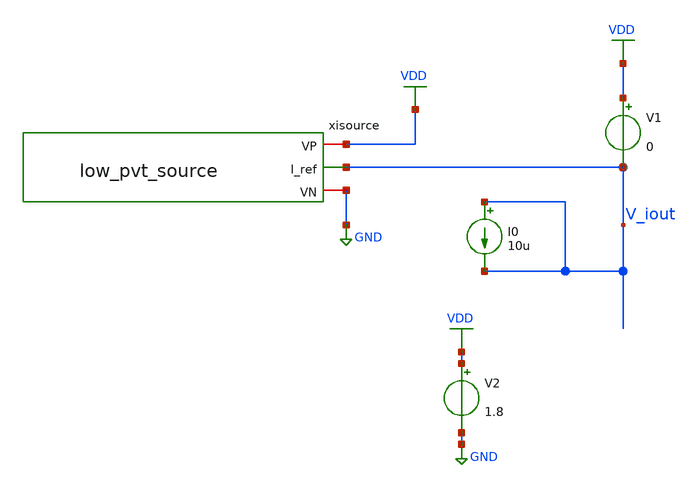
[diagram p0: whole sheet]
** sch_path: xschem/test/test_low_pvt_source.sch
**.subckt test_low_pvt_source
V2 VDD GND 1.8
V1 VDD V_iout 0
xisource VDD V_iout GND low_pvt_source
I0 V_iout V_iout 10u
**** begin user architecture code


*.options savecurrents
.option warn=1
.control
set wr_vecnames
set wr_singlescale
set hcopydevtype=svg
set ITL1=10000

let min_temp=0
let var_temp = min_temp
let max_temp=100
let temp_step=100

option temp=20
op
write test_low_pvt_source.raw
print var_temp i(v1)
*  i(v.xisource.v1)
run
reset



dowhile var_temp <= max_temp
	option temp=$&var_temp
	op
	* wrdata 'result_{$&var_temp}deg.csv' v(V_vout)
	let var_temp = var_temp + temp_step
	run
	echo 'Result will follow ...'
	print var_temp  i(v1)
	* i(v.xisource.v1)
	if i(v.xisource.v1) > 1e-6
		echo 'Large current'
		write 'result_op_{$&var_temp}deg.raw'
	end
	*tran 100n 100u
	*MEAS tran isource AVG i(v.xisource.v1) from=50u to=100u
	reset
end

* reset
* option temp=0
* op
* run
* print v(v_vout) i(v1)
* let var_vout_0deg=v(v_vout)
* reset
* option temp=100
* op
* run
* print v(v_vout) i(v1)
* let var_vout_100deg=v(v_vout)

* print var_vout_100deg-var_vout_0deg

* tran 100n 100u
* plot i(v.xisource.v1)
* MEAS tran isource AVG i(v.xisource.v1) from=50u to=100u
* noise i(v1) I0 dec 1000 10 100G
* print all
* wrdata result_noise.csv inoise_total onoise_total
* setplot noise1
* plot onoise_spectrum
* noise i(v1) I0 dec 1000 2MEG 2G
* print all
* wrdata result_noise.csv inoise_total onoise_total
* setplot noise3
* plot onoise_spectrum


.endc




* .include ../../tia.spice
* .include ../../filter_diff.spice
* .include ../../cmm_sense3.spice

.include low_pvt_source.spice



* .lib $::SKYWATER_MODELS/sky130.lib.spice hl
.lib $::SKYWATER_MODELS/sky130.lib.spice.tt.red tt
* .lib /home/simon/share/pdk/sky130A/libs.tech/ngspice/sky130.lib.spice.tt.red tt

**** end user architecture code
**.ends

* expanding   symbol:  /home/simon/code/asic/analog/bias/low_pvt_source.sym # of pins=3
** sym_path: xschem/bias/low_pvt_source.sym
** sch_path: xschem/bias/low_pvt_source.sch
.subckt low_pvt_source VP I_ref VN
*.iopin VP
*.opin I_ref
*.iopin VN
XM1 VM1D VM8D VP VP sky130_fd_pr__pfet_01v8 L=1 W=4 nf=1 ad='int((nf+1)/2) * W/nf * 0.29' as='int((nf+2)/2) * W/nf * 0.29'
+ pd='2*int((nf+1)/2) * (W/nf + 0.29)' ps='2*int((nf+2)/2) * (W/nf + 0.29)' nrd='0.29 / W' nrs='0.29 / W'
+ sa=0 sb=0 sd=0 mult=10 m=10
XM2 VM2D VM2D VN VN sky130_fd_pr__nfet_01v8 L=6 W=4 nf=1 ad='int((nf+1)/2) * W/nf * 0.29' as='int((nf+2)/2) * W/nf * 0.29'
+ pd='2*int((nf+1)/2) * (W/nf + 0.29)' ps='2*int((nf+2)/2) * (W/nf + 0.29)' nrd='0.29 / W' nrs='0.29 / W'
+ sa=0 sb=0 sd=0 mult=30 m=30
XM5 VM9D VM8D VM1D VP sky130_fd_pr__pfet_01v8 L=0.2 W=4 nf=1 ad='int((nf+1)/2) * W/nf * 0.29' as='int((nf+2)/2) * W/nf * 0.29'
+ pd='2*int((nf+1)/2) * (W/nf + 0.29)' ps='2*int((nf+2)/2) * (W/nf + 0.29)' nrd='0.29 / W' nrs='0.29 / W'
+ sa=0 sb=0 sd=0 mult=2 m=2
XM11 VM11D VM2D VM12D VN sky130_fd_pr__nfet_01v8 L=6 W=4 nf=1 ad='int((nf+1)/2) * W/nf * 0.29' as='int((nf+2)/2) * W/nf * 0.29'
+ pd='2*int((nf+1)/2) * (W/nf + 0.29)' ps='2*int((nf+2)/2) * (W/nf + 0.29)' nrd='0.29 / W' nrs='0.29 / W'
+ sa=0 sb=0 sd=0 mult=65 m=65
XM12 VM12D VM12G VN VN sky130_fd_pr__nfet_01v8 L=6 W=4 nf=1 ad='int((nf+1)/2) * W/nf * 0.29' as='int((nf+2)/2) * W/nf * 0.29'
+ pd='2*int((nf+1)/2) * (W/nf + 0.29)' ps='2*int((nf+2)/2) * (W/nf + 0.29)' nrd='0.29 / W' nrs='0.29 / W'
+ sa=0 sb=0 sd=0 mult=2 m=2
XM14 VM14D VM12G VN VN sky130_fd_pr__nfet_01v8 L=6 W=4 nf=1 ad='int((nf+1)/2) * W/nf * 0.29' as='int((nf+2)/2) * W/nf * 0.29'
+ pd='2*int((nf+1)/2) * (W/nf + 0.29)' ps='2*int((nf+2)/2) * (W/nf + 0.29)' nrd='0.29 / W' nrs='0.29 / W'
+ sa=0 sb=0 sd=0 mult=2 m=2
XM16 VM16D VM8D VP VP sky130_fd_pr__pfet_01v8 L=1 W=4 nf=1 ad='int((nf+1)/2) * W/nf * 0.29' as='int((nf+2)/2) * W/nf * 0.29'
+ pd='2*int((nf+1)/2) * (W/nf + 0.29)' ps='2*int((nf+2)/2) * (W/nf + 0.29)' nrd='0.29 / W' nrs='0.29 / W'
+ sa=0 sb=0 sd=0 mult=10 m=10
XM17 VM8D VM8D VM16D VP sky130_fd_pr__pfet_01v8 L=0.2 W=4 nf=1 ad='int((nf+1)/2) * W/nf * 0.29' as='int((nf+2)/2) * W/nf * 0.29'
+ pd='2*int((nf+1)/2) * (W/nf + 0.29)' ps='2*int((nf+2)/2) * (W/nf + 0.29)' nrd='0.29 / W' nrs='0.29 / W'
+ sa=0 sb=0 sd=0 mult=2 m=2
XM18 VM18D VM8D VP VP sky130_fd_pr__pfet_01v8 L=1 W=4 nf=1 ad='int((nf+1)/2) * W/nf * 0.29' as='int((nf+2)/2) * W/nf * 0.29'
+ pd='2*int((nf+1)/2) * (W/nf + 0.29)' ps='2*int((nf+2)/2) * (W/nf + 0.29)' nrd='0.29 / W' nrs='0.29 / W'
+ sa=0 sb=0 sd=0 mult=10*3*2 m=10*3*2
XM19 VM14D VM8D VM18D VP sky130_fd_pr__pfet_01v8 L=0.2 W=4 nf=1 ad='int((nf+1)/2) * W/nf * 0.29' as='int((nf+2)/2) * W/nf * 0.29'
+ pd='2*int((nf+1)/2) * (W/nf + 0.29)' ps='2*int((nf+2)/2) * (W/nf + 0.29)' nrd='0.29 / W' nrs='0.29 / W'
+ sa=0 sb=0 sd=0 mult=2*3*2 m=2*3*2
XM20 VM20D VM8D VP VP sky130_fd_pr__pfet_01v8 L=1 W=4 nf=1 ad='int((nf+1)/2) * W/nf * 0.29' as='int((nf+2)/2) * W/nf * 0.29'
+ pd='2*int((nf+1)/2) * (W/nf + 0.29)' ps='2*int((nf+2)/2) * (W/nf + 0.29)' nrd='0.29 / W' nrs='0.29 / W'
+ sa=0 sb=0 sd=0 mult=10*1*1 m=10*1*1
XM21 VM22D VM8D VM20D VP sky130_fd_pr__pfet_01v8 L=0.2 W=4 nf=1 ad='int((nf+1)/2) * W/nf * 0.29' as='int((nf+2)/2) * W/nf * 0.29'
+ pd='2*int((nf+1)/2) * (W/nf + 0.29)' ps='2*int((nf+2)/2) * (W/nf + 0.29)' nrd='0.29 / W' nrs='0.29 / W'
+ sa=0 sb=0 sd=0 mult=2*1*1 m=2*1*1
XM22 VM22D VM4S VM3D VN sky130_fd_pr__nfet_01v8 L=6 W=4 nf=1 ad='int((nf+1)/2) * W/nf * 0.29' as='int((nf+2)/2) * W/nf * 0.29'
+ pd='2*int((nf+1)/2) * (W/nf + 0.29)' ps='2*int((nf+2)/2) * (W/nf + 0.29)' nrd='0.29 / W' nrs='0.29 / W'
+ sa=0 sb=0 sd=0 mult=20 m=20
XM3 VM3D VM3G VN VN sky130_fd_pr__nfet_01v8 L=6 W=4 nf=1 ad='int((nf+1)/2) * W/nf * 0.29' as='int((nf+2)/2) * W/nf * 0.29'
+ pd='2*int((nf+1)/2) * (W/nf + 0.29)' ps='2*int((nf+2)/2) * (W/nf + 0.29)' nrd='0.29 / W' nrs='0.29 / W'
+ sa=0 sb=0 sd=0 mult=4 m=4
XM13 VP VM14D VM12G VM12G sky130_fd_pr__nfet_01v8_lvt L=0.15 W=4 nf=1 ad='int((nf+1)/2) * W/nf * 0.29'
+ as='int((nf+2)/2) * W/nf * 0.29' pd='2*int((nf+1)/2) * (W/nf + 0.29)' ps='2*int((nf+2)/2) * (W/nf + 0.29)'
+ nrd='0.29 / W' nrs='0.29 / W' sa=0 sb=0 sd=0 mult=20 m=20
XM4 I_ref VM22D VM4S VN sky130_fd_pr__nfet_01v8_lvt L=0.15 W=4 nf=1 ad='int((nf+1)/2) * W/nf * 0.29'
+ as='int((nf+2)/2) * W/nf * 0.29' pd='2*int((nf+1)/2) * (W/nf + 0.29)' ps='2*int((nf+2)/2) * (W/nf + 0.29)'
+ nrd='0.29 / W' nrs='0.29 / W' sa=0 sb=0 sd=0 mult=20 m=20
XM48 VM50D VM11D VP VP sky130_fd_pr__pfet_01v8 L=2 W=0.5 nf=1 ad='int((nf+1)/2) * W/nf * 0.29' as='int((nf+2)/2) * W/nf * 0.29'
+ pd='2*int((nf+1)/2) * (W/nf + 0.29)' ps='2*int((nf+2)/2) * (W/nf + 0.29)' nrd='0.29 / W' nrs='0.29 / W'
+ sa=0 sb=0 sd=0 mult=1 m=1
XM50 VM50D VM11D VN VN sky130_fd_pr__nfet_01v8_lvt L=0.2 W=4 nf=1 ad='int((nf+1)/2) * W/nf * 0.29' as='int((nf+2)/2) * W/nf * 0.29'
+ pd='2*int((nf+1)/2) * (W/nf + 0.29)' ps='2*int((nf+2)/2) * (W/nf + 0.29)' nrd='0.29 / W' nrs='0.29 / W'
+ sa=0 sb=0 sd=0 mult=10 m=10
XC3 VP VM8D sky130_fd_pr__cap_mim_m3_1 W=20 L=20 MF=1 m=1
XM8 VM8D VM9D VM11D VM11D sky130_fd_pr__nfet_01v8_lvt L=1 W=4 nf=1 ad='int((nf+1)/2) * W/nf * 0.29' as='int((nf+2)/2) * W/nf * 0.29'
+ pd='2*int((nf+1)/2) * (W/nf + 0.29)' ps='2*int((nf+2)/2) * (W/nf + 0.29)' nrd='0.29 / W' nrs='0.29 / W'
+ sa=0 sb=0 sd=0 mult=20 m=20
XM9 VM9D VM9D VM2D VM2D sky130_fd_pr__nfet_01v8_lvt L=1 W=4 nf=1 ad='int((nf+1)/2) * W/nf * 0.29' as='int((nf+2)/2) * W/nf * 0.29'
+ pd='2*int((nf+1)/2) * (W/nf + 0.29)' ps='2*int((nf+2)/2) * (W/nf + 0.29)' nrd='0.29 / W' nrs='0.29 / W'
+ sa=0 sb=0 sd=0 mult=20 m=20
XM10 VM8D VM50D VN VN sky130_fd_pr__nfet_01v8 L=2 W=0.5 nf=1 ad='int((nf+1)/2) * W/nf * 0.29' as='int((nf+2)/2) * W/nf * 0.29'
+ pd='2*int((nf+1)/2) * (W/nf + 0.29)' ps='2*int((nf+2)/2) * (W/nf + 0.29)' nrd='0.29 / W' nrs='0.29 / W'
+ sa=0 sb=0 sd=0 mult=1 m=1
XC4 VN VP sky130_fd_pr__cap_mim_m3_2 W=30 L=30 MF=1 m=1
XR7 net3 VM4S VN sky130_fd_pr__res_xhigh_po_1p41 L=10 mult=1 m=1
XR3 net4 net3 VN sky130_fd_pr__res_xhigh_po_1p41 L=10 mult=1 m=1
XR4 net2 net4 VN sky130_fd_pr__res_xhigh_po_1p41 L=10 mult=1 m=1
XR5 net1 net2 VN sky130_fd_pr__res_xhigh_po_1p41 L=10 mult=1 m=1
XR6 VN net1 VN sky130_fd_pr__res_xhigh_po_1p41 L=10 mult=1 m=1
XR8 net5 VM12G VN sky130_fd_pr__res_xhigh_po_1p41 L=10 mult=1 m=1
XR1 net5 VM3G VN sky130_fd_pr__res_xhigh_po_1p41 L=10 mult=1 m=1
XR2 net7 net6 VN sky130_fd_pr__res_xhigh_po_1p41 L=10 mult=1 m=1
XR9 VN net6 VN sky130_fd_pr__res_xhigh_po_1p41 L=10 mult=1 m=1
XR10 net11 net7 VN sky130_fd_pr__res_xhigh_po_1p41 L=10 mult=1 m=1
XR11 net12 net11 VN sky130_fd_pr__res_xhigh_po_1p41 L=10 mult=1 m=1
XR12 net8 net12 VN sky130_fd_pr__res_xhigh_po_1p41 L=10 mult=1 m=1
XR13 net10 VM3G VN sky130_fd_pr__res_xhigh_po_1p41 L=10 mult=1 m=1
XR14 net9 net10 VN sky130_fd_pr__res_xhigh_po_1p41 L=10 mult=1 m=1
XR15 net8 net9 VN sky130_fd_pr__res_xhigh_po_1p41 L=10 mult=1 m=1
XC1 VN VP sky130_fd_pr__cap_mim_m3_2 W=30 L=30 MF=1 m=1
.ends

.GLOBAL VDD
.GLOBAL GND
.end
